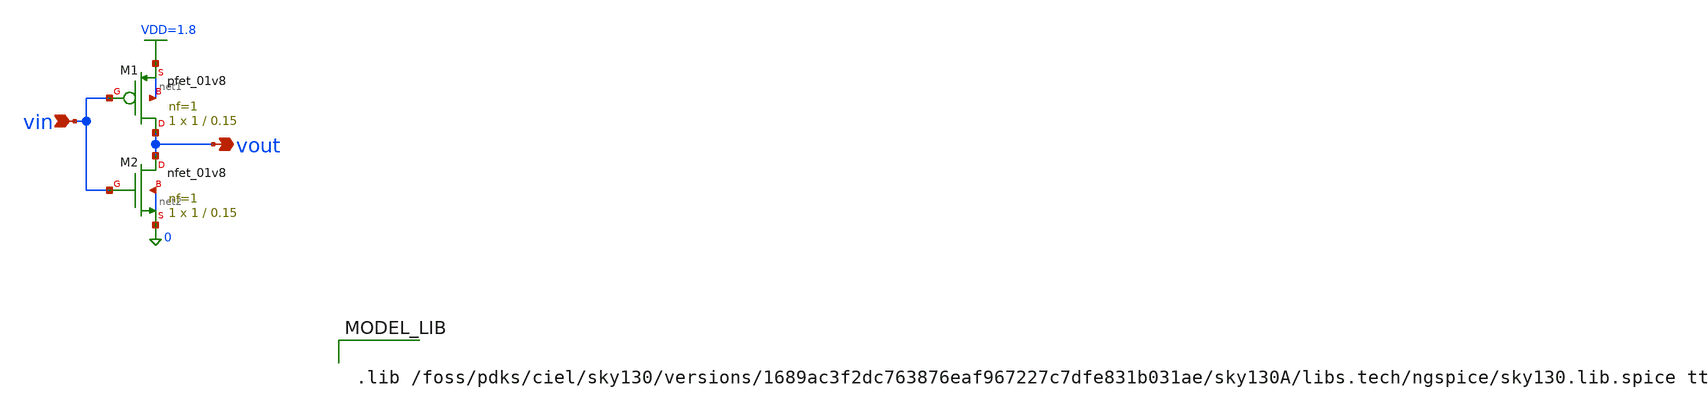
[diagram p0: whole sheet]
** sch_path: Lab1-Warmup-Xschem/inverter.sch
**.subckt inverter vin vout
*.ipin vin
*.opin vout
XM1 vout vin VDD=1.8 net1 sky130_fd_pr__pfet_01v8 L=0.15 W=1 nf=1 ad='int((1 + 1)/2) * 1 / 1 * 0.29'
+ as='int((1 + 2)/2) * 1 / 1 * 0.29' pd='2*int((1 + 1)/2) * (1 / 1 + 0.29)' ps='2*int((1 + 2)/2) * (1 / 1 + 0.29)'
+ nrd='0.29 / 1 ' nrs='0.29 / 1 ' sa=0 sb=0 sd=0 mult=1 m=1
XM2 vout vin 0 net2 sky130_fd_pr__nfet_01v8 L=0.15 W=1 nf=1 ad='int((1 + 1)/2) * 1 / 1 * 0.29' as='int((1 + 2)/2) * 1 / 1 * 0.29'
+ pd='2*int((1 + 1)/2) * (1 / 1 + 0.29)' ps='2*int((1 + 2)/2) * (1 / 1 + 0.29)' nrd='0.29 / 1 ' nrs='0.29 / 1 '
+ sa=0 sb=0 sd=0 mult=1 m=1
**** begin user architecture code


.lib /foss/pdks/ciel/sky130/versions/1689ac3f2dc763876eaf967227c7dfe831b031ae/sky130A/libs.tech/ngspice/sky130.lib.spice tt


**** end user architecture code
**.ends
.GLOBAL VDD=1.8
.end
